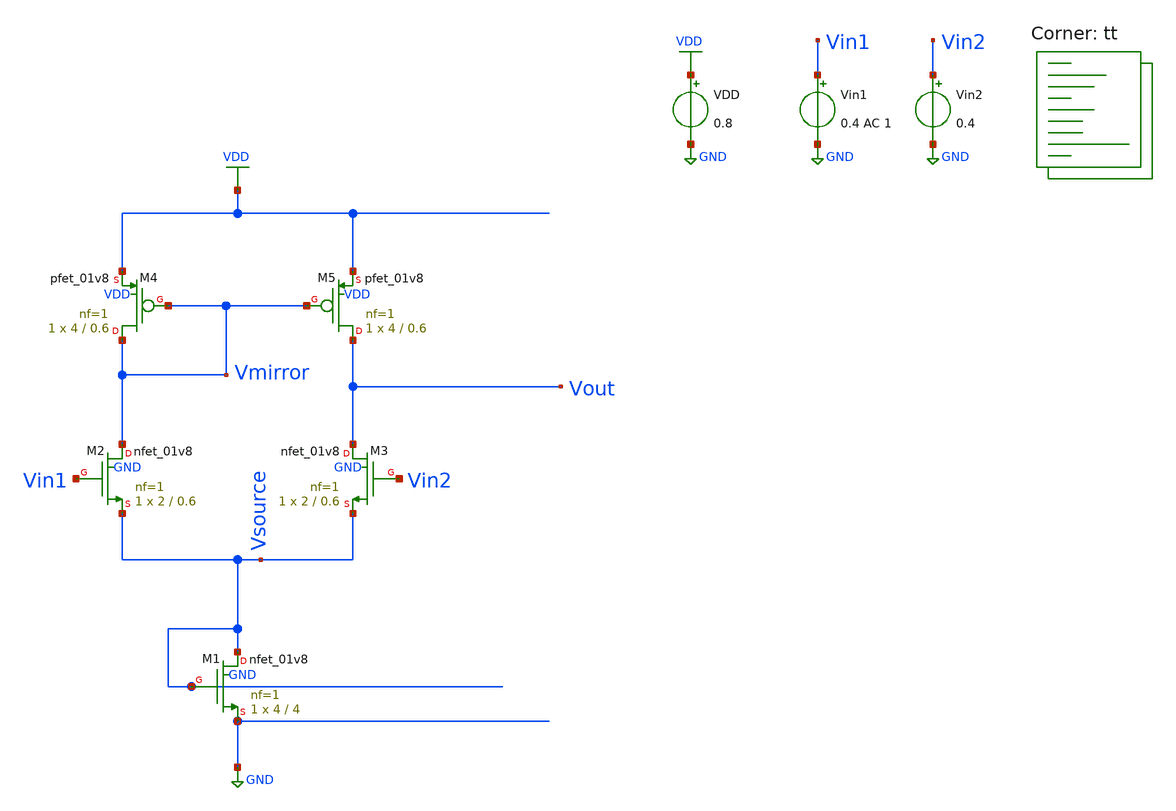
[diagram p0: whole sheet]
** sch_path: projects/pll/bandgapref/xschem_ngspice/tb_opamp_bandgap2.sch
**.subckt tb_opamp_bandgap2
VDD VDD GND 0.8
Vin1 Vin1 GND 0.4 AC 1
Vin2 Vin2 GND 0.4
XM1 Vsource Vsource GND GND sky130_fd_pr__nfet_01v8 L=4 W=4 nf=1 ad='int((nf+1)/2) * W/nf * 0.29' as='int((nf+2)/2) * W/nf * 0.29'
+ pd='2*int((nf+1)/2) * (W/nf + 0.29)' ps='2*int((nf+2)/2) * (W/nf + 0.29)' nrd='0.29 / W' nrs='0.29 / W'
+ sa=0 sb=0 sd=0 mult=1 m=1
XM2 Vmirror Vin1 Vsource GND sky130_fd_pr__nfet_01v8 L=0.6 W=2 nf=1 ad='int((nf+1)/2) * W/nf * 0.29'
+ as='int((nf+2)/2) * W/nf * 0.29' pd='2*int((nf+1)/2) * (W/nf + 0.29)' ps='2*int((nf+2)/2) * (W/nf + 0.29)'
+ nrd='0.29 / W' nrs='0.29 / W' sa=0 sb=0 sd=0 mult=1 m=1
XM3 Vout Vin2 Vsource GND sky130_fd_pr__nfet_01v8 L=0.6 W=2 nf=1 ad='int((nf+1)/2) * W/nf * 0.29' as='int((nf+2)/2) * W/nf * 0.29'
+ pd='2*int((nf+1)/2) * (W/nf + 0.29)' ps='2*int((nf+2)/2) * (W/nf + 0.29)' nrd='0.29 / W' nrs='0.29 / W'
+ sa=0 sb=0 sd=0 mult=1 m=1
XM4 Vmirror Vmirror VDD VDD sky130_fd_pr__pfet_01v8 L=0.6 W=4 nf=1 ad='int((nf+1)/2) * W/nf * 0.29' as='int((nf+2)/2) * W/nf * 0.29'
+ pd='2*int((nf+1)/2) * (W/nf + 0.29)' ps='2*int((nf+2)/2) * (W/nf + 0.29)' nrd='0.29 / W' nrs='0.29 / W'
+ sa=0 sb=0 sd=0 mult=1 m=1
XM5 Vout Vmirror VDD VDD sky130_fd_pr__pfet_01v8 L=0.6 W=4 nf=1 ad='int((nf+1)/2) * W/nf * 0.29' as='int((nf+2)/2) * W/nf * 0.29'
+ pd='2*int((nf+1)/2) * (W/nf + 0.29)' ps='2*int((nf+2)/2) * (W/nf + 0.29)' nrd='0.29 / W' nrs='0.29 / W'
+ sa=0 sb=0 sd=0 mult=1 m=1
**** begin user architecture code



.option method=gear
.option wnflag=1
.option savecurrents

.save @m.xm1.msky130_fd_pr__nfet_01v8[gm] @m.xm2.msky130_fd_pr__nfet_01v8[gm] @m.xm3.msky130_fd_pr__nfet_01v8[gm] @m.xm4.msky130_fd_pr__pfet_01v8[gm] @m.xm5.msky130_fd_pr__pfet_01v8[gm] @m.xm6.msky130_fd_pr__pfet_01v8[gm] @m.xm7.msky130_fd_pr__nfet_01v8[gm]


.control

  save all
  *tran 1u 20m
  ac dec 20 1 1T
  remzerovec
  write tb_opamp_bandgap2.raw
  set appendwrite

.endc



.lib $::SKYWATER_MODELS/sky130.lib.spice tt
**** end user architecture code
**.ends
.GLOBAL GND
.GLOBAL VDD
.end
